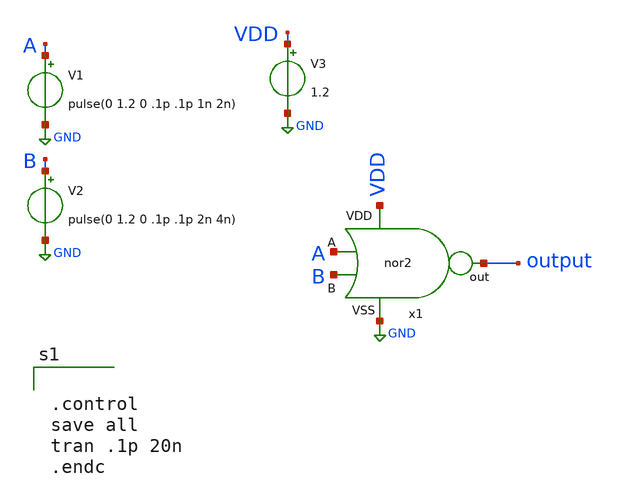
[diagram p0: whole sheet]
** sch_path: nor/nor2_tb.sch
**.subckt nor2_tb
x1 VDD A B output GND nor2
V1 A GND pulse(0 1.2 0 .1p .1p 1n 2n)
V2 B GND pulse(0 1.2 0 .1p .1p 2n 4n)
V3 VDD GND 1.2
**** begin user architecture code

** opencircuitdesign pdks install
.lib $::SKYWATER_MODELS/sky130.lib.spice tt




.control
save all
tran .1p 20n
.endc

**** end user architecture code
**.ends

* expanding   symbol:  nor2.sym # of pins=5
** sym_path: nor/nor2.sym
** sch_path: nor/nor2.sch
.subckt nor2 VDD A B out VSS
*.ipin A
*.ipin B
*.opin out
*.ipin VSS
*.ipin VDD
XM1 out B VSS VSS sky130_fd_pr__nfet_01v8 L=0.15 W=1 nf=1 ad='int((nf+1)/2) * W/nf * 0.29' as='int((nf+2)/2) * W/nf * 0.29'
+ pd='2*int((nf+1)/2) * (W/nf + 0.29)' ps='2*int((nf+2)/2) * (W/nf + 0.29)' nrd='0.29 / W' nrs='0.29 / W'
+ sa=0 sb=0 sd=0 mult=1 m=1
XM2 out B net1 net1 sky130_fd_pr__pfet_01v8 L=0.15 W=1 nf=1 ad='int((nf+1)/2) * W/nf * 0.29' as='int((nf+2)/2) * W/nf * 0.29'
+ pd='2*int((nf+1)/2) * (W/nf + 0.29)' ps='2*int((nf+2)/2) * (W/nf + 0.29)' nrd='0.29 / W' nrs='0.29 / W'
+ sa=0 sb=0 sd=0 mult=1 m=1
XM3 net1 A VDD VDD sky130_fd_pr__pfet_01v8 L=0.15 W=1 nf=1 ad='int((nf+1)/2) * W/nf * 0.29' as='int((nf+2)/2) * W/nf * 0.29'
+ pd='2*int((nf+1)/2) * (W/nf + 0.29)' ps='2*int((nf+2)/2) * (W/nf + 0.29)' nrd='0.29 / W' nrs='0.29 / W'
+ sa=0 sb=0 sd=0 mult=1 m=1
XM4 out A VSS VSS sky130_fd_pr__nfet_01v8 L=0.15 W=1 nf=1 ad='int((nf+1)/2) * W/nf * 0.29' as='int((nf+2)/2) * W/nf * 0.29'
+ pd='2*int((nf+1)/2) * (W/nf + 0.29)' ps='2*int((nf+2)/2) * (W/nf + 0.29)' nrd='0.29 / W' nrs='0.29 / W'
+ sa=0 sb=0 sd=0 mult=1 m=1
.ends

.GLOBAL GND
.end
